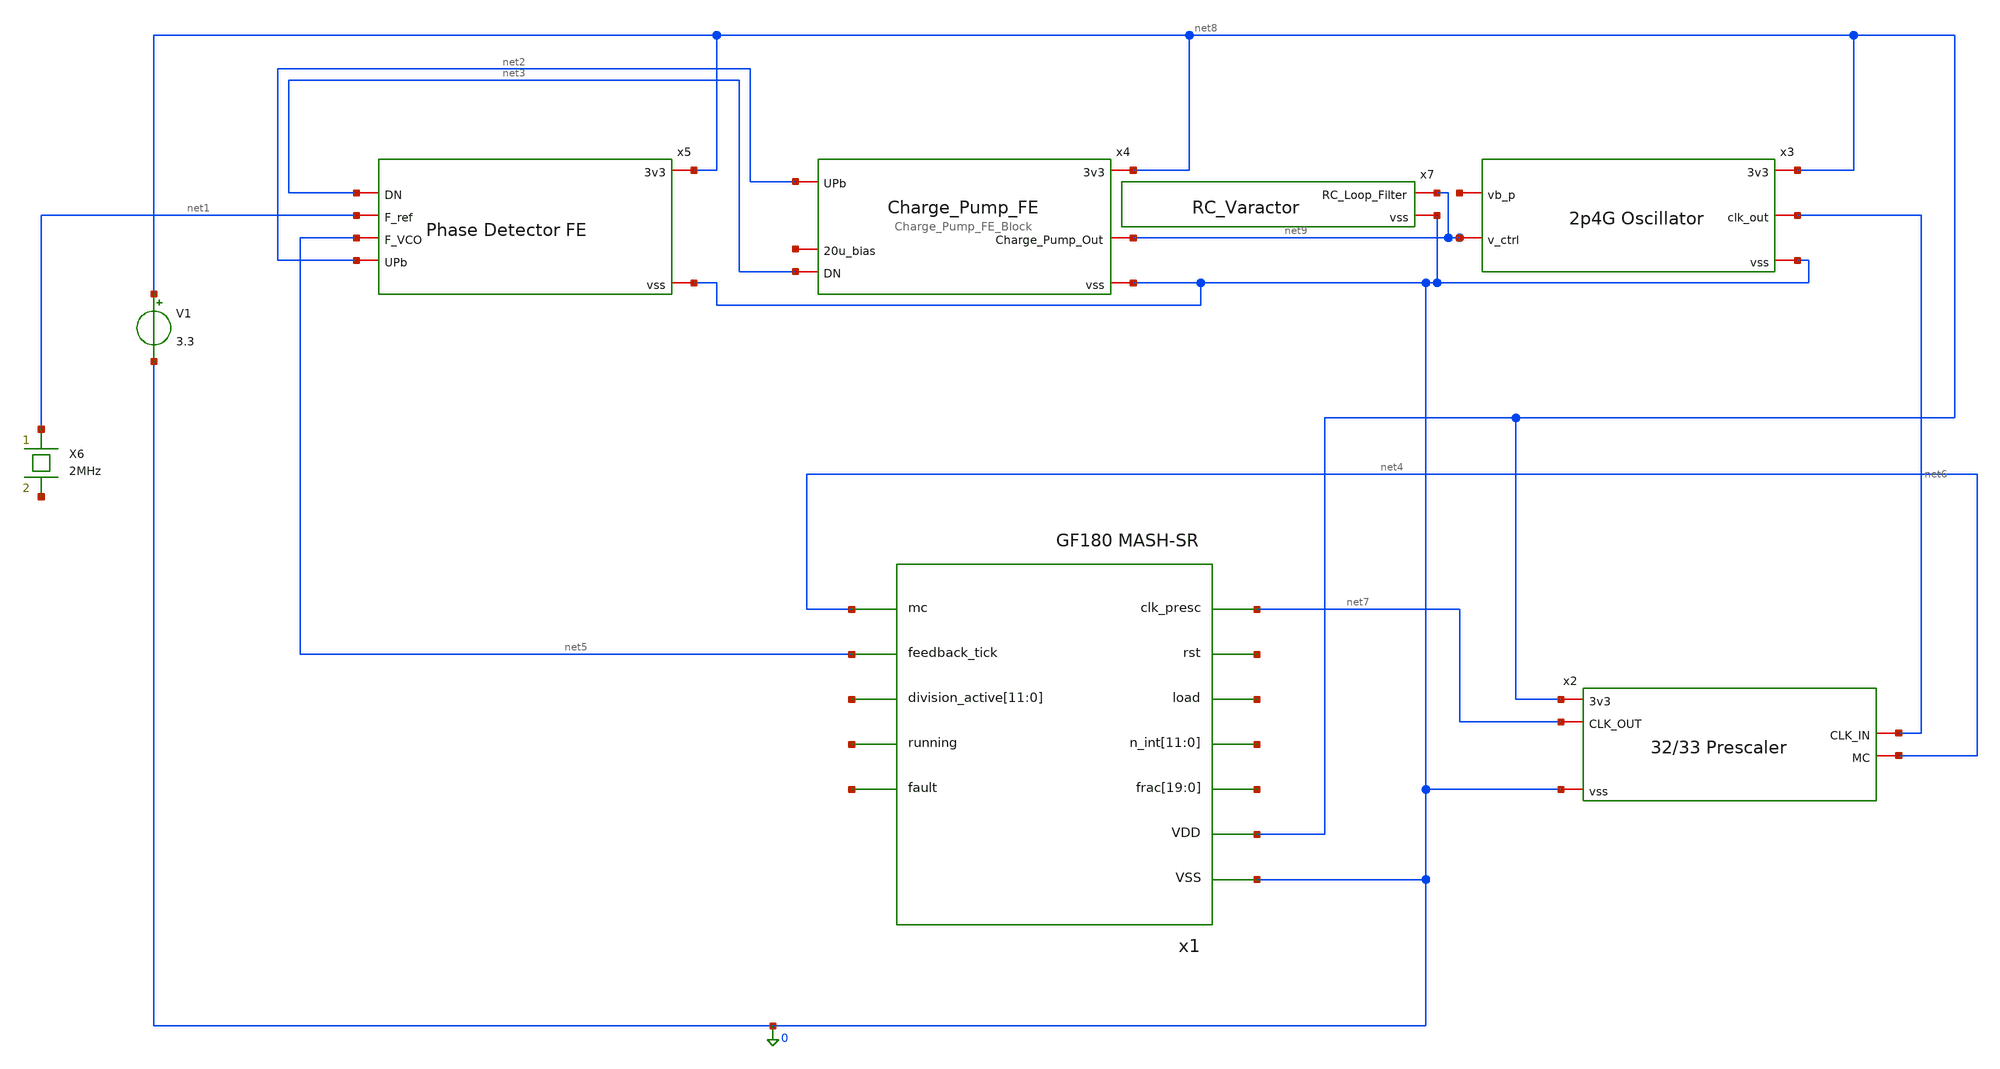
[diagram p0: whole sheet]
** sch_path: PLL/analog/schematics/PLL.sch
**.subckt PLL
x1 net7 net10 net11 net12[11] net12[10] net12[9] net12[8] net12[7] net12[6] net12[5] net12[4]
+ net12[3] net12[2] net12[1] net12[0] net13[19] net13[18] net13[17] net13[16] net13[15] net13[14] net13[13]
+ net13[12] net13[11] net13[10] net13[9] net13[8] net13[7] net13[6] net13[5] net13[4] net13[3] net13[2]
+ net13[1] net13[0] net4 net5 net14[11] net14[10] net14[9] net14[8] net14[7] net14[6] net14[5] net14[4]
+ net14[3] net14[2] net14[1] net14[0] net15 net16 net8 0 fractional_32_33
x2 net8 net7 net6 net4 0 32_33_Prescaler_Block
x3 net8 net17 net6 net9 0 Ring_Oscillator_Block
x4 net8 net2 net18 net9 net3 0 Charge_Pump_FE_Block
X6 net1 net19 crystal
V1 net8 0 3.3
x7 net9 0 RC_Varactor
x5 net8 net3 net1 net5 net2 0 Phase_Detector_Block
**.ends
.end
